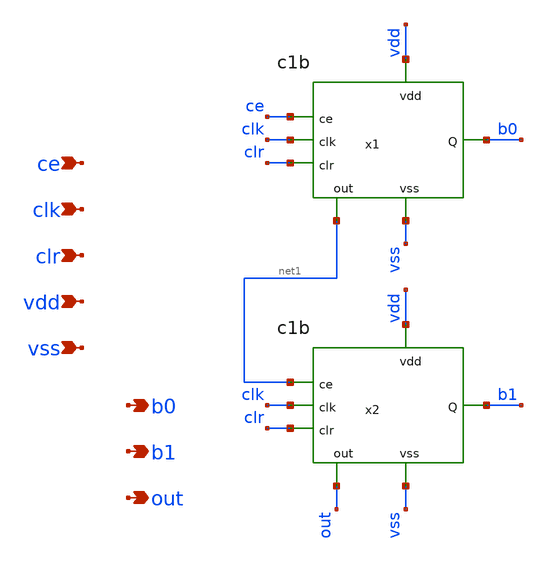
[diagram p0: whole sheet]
** sch_path: track_vlsi/martinez-sapriza/sch/c2b.sch
**.subckt c2b ce clk clr vdd vss b1 b0 out
*.ipin ce
*.ipin clk
*.ipin clr
*.ipin vdd
*.ipin vss
*.opin b1
*.opin b0
*.opin out
x1 ce clk clr vdd vss b0 net1 c1b
x2 net1 clk clr vdd vss b1 out c1b
**.ends
.end
